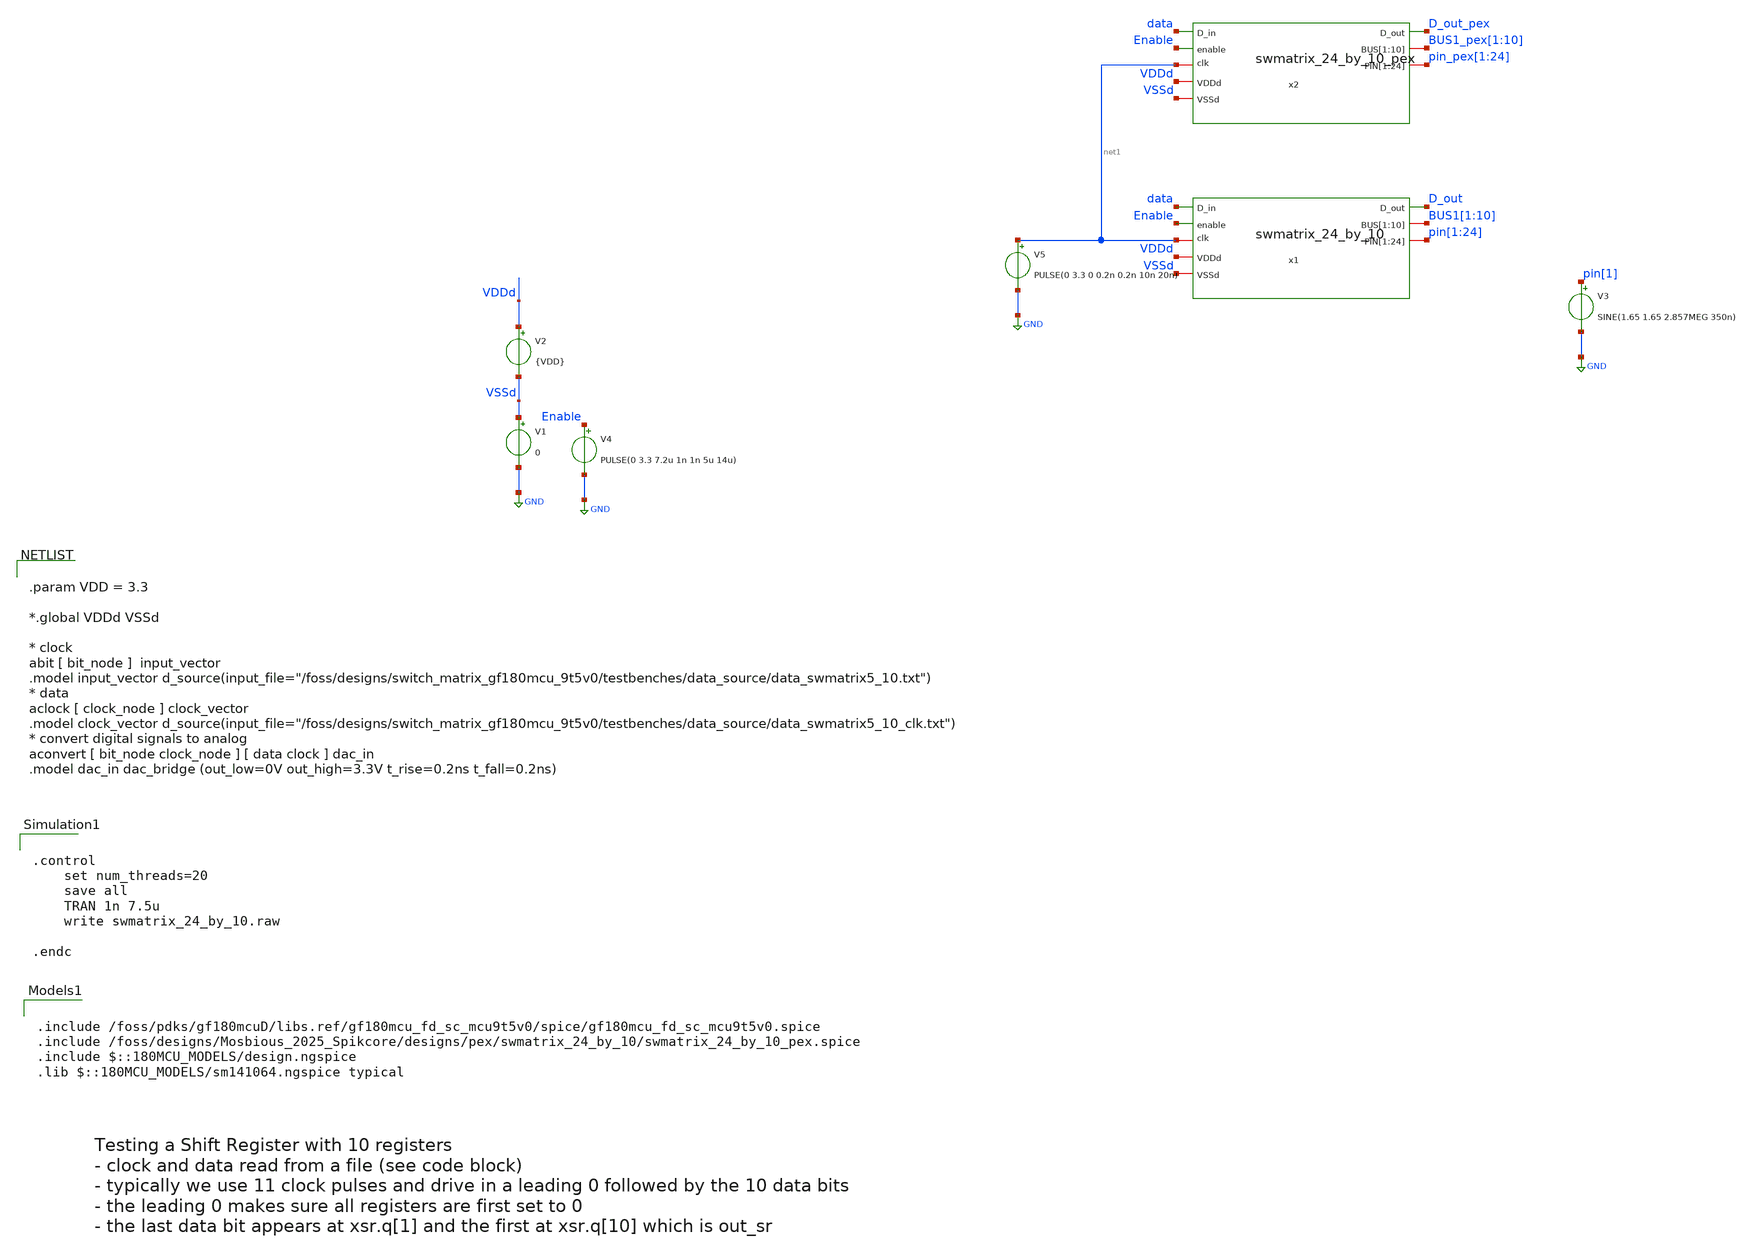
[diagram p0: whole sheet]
** sch_path: designs/pex/swmatrix_24_by_10/swmatrix_24_by_10_pex.sch
**.subckt swmatrix_24_by_10_pex
V1 VSSd GND 0
V2 VDDd VSSd {VDD}
V3 pin[1] GND SINE(1.65 1.65 2.857MEG 350n)
V4 Enable GND PULSE(0 3.3 7.2u 1n 1n 5u 14u)
x1 D_out BUS1[1] BUS1[2] BUS1[3] BUS1[4] BUS1[5] BUS1[6] BUS1[7] BUS1[8] BUS1[9] BUS1[10] pin[1]
+ pin[2] pin[3] pin[4] pin[5] pin[6] pin[7] pin[8] pin[9] pin[10] pin[11] pin[12] pin[13] pin[14] pin[15]
+ pin[16] pin[17] pin[18] pin[19] pin[20] pin[21] pin[22] pin[23] pin[24] data VDDd Enable VSSd net1
+ swmatrix_24_by_10
V5 net1 GND PULSE(0 3.3 0 0.2n 0.2n 10n 20n)
x2 D_out_pex BUS1_pex[1] BUS1_pex[2] BUS1_pex[3] BUS1_pex[4] BUS1_pex[5] BUS1_pex[6] BUS1_pex[7]
+ BUS1_pex[8] BUS1_pex[9] BUS1_pex[10] pin_pex[1] pin_pex[2] pin_pex[3] pin_pex[4] pin_pex[5] pin_pex[6]
+ pin_pex[7] pin_pex[8] pin_pex[9] pin_pex[10] pin_pex[11] pin_pex[12] pin_pex[13] pin_pex[14] pin_pex[15]
+ pin_pex[16] pin_pex[17] pin_pex[18] pin_pex[19] pin_pex[20] pin_pex[21] pin_pex[22] pin_pex[23] pin_pex[24]
+ data VDDd Enable VSSd net1 swmatrix_24_by_10_pex
**** begin user architecture code


.param VDD = 3.3

*.global VDDd VSSd

* clock
abit [ bit_node ]  input_vector
.model input_vector
+ d_source(input_file="/foss/designs/switch_matrix_gf180mcu_9t5v0/testbenches/data_source/data_swmatrix5_10.txt")
* data
aclock [ clock_node ] clock_vector
.model clock_vector
+ d_source(input_file="/foss/designs/switch_matrix_gf180mcu_9t5v0/testbenches/data_source/data_swmatrix5_10_clk.txt")
* convert digital signals to analog
aconvert [ bit_node clock_node ] [ data clock ] dac_in
.model dac_in dac_bridge (out_low=0V out_high=3.3V t_rise=0.2ns t_fall=0.2ns)




.control
    set num_threads=20
    save all
    TRAN 1n 7.5u
    write swmatrix_24_by_10.raw

.endc



.include /foss/pdks/gf180mcuD/libs.ref/gf180mcu_fd_sc_mcu9t5v0/spice/gf180mcu_fd_sc_mcu9t5v0.spice
.include /foss/designs/Mosbious_2025_Spikcore/designs/pex/swmatrix_24_by_10/swmatrix_24_by_10_pex.spice
.include $::180MCU_MODELS/design.ngspice
.lib $::180MCU_MODELS/sm141064.ngspice typical

**** end user architecture code
**.ends
.GLOBAL GND
.end
